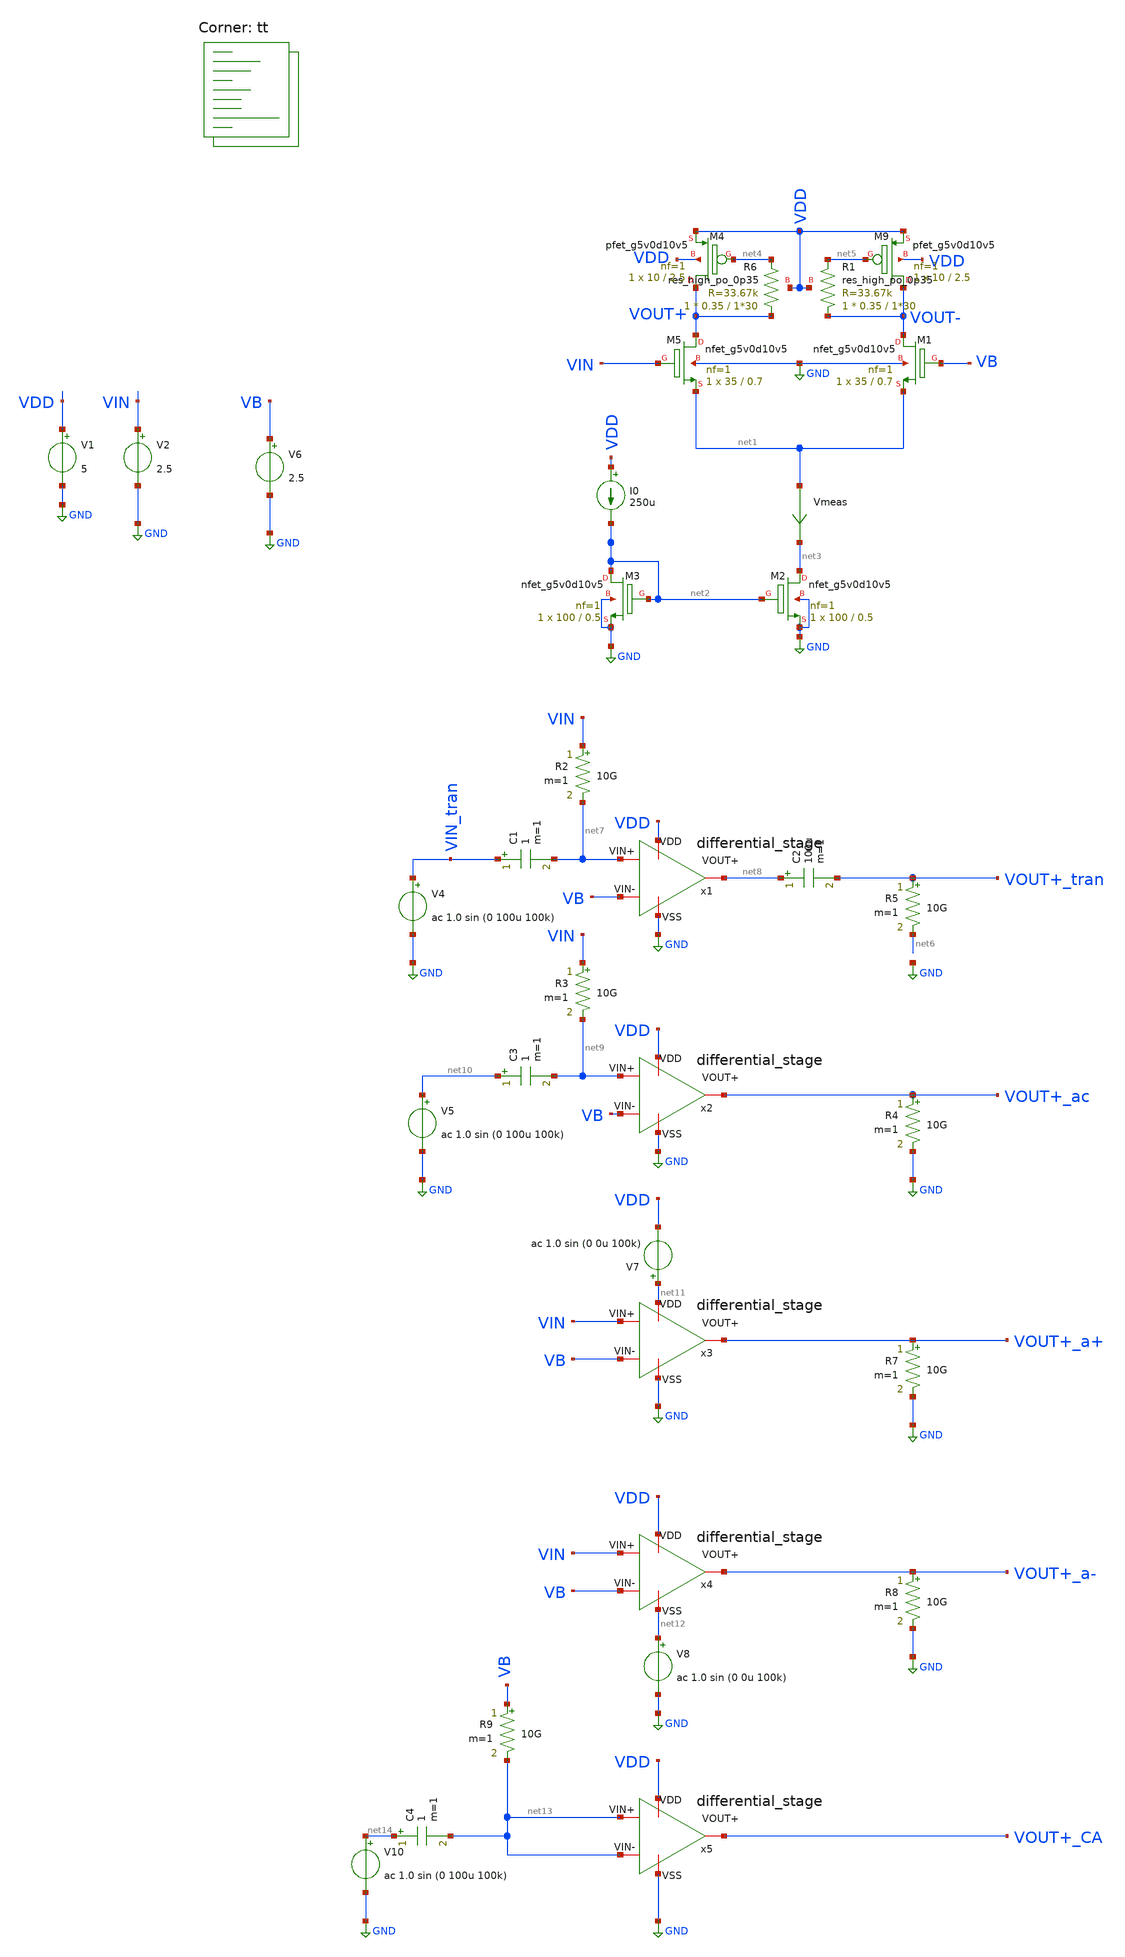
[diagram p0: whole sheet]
** sch_path: amplifiers/differencial_stage_amps/basic_stages/basic_NMOS_dif_stage/diferential_stage.sch
**.subckt diferential_stage
XM5 VOUT+ VIN net1 GND sky130_fd_pr__nfet_g5v0d10v5 L=0.7 W=35 nf=1 ad='int((1 + 1)/2) * 35 / 1 * 0.29'
+ as='int((1 + 2)/2) * 35 / 1 * 0.29' pd='2*int((1 + 1)/2) * (35 / 1 + 0.29)' ps='2*int((1 + 2)/2) * (35 / 1 + 0.29)'
+ nrd='0.29 / 35 ' nrs='0.29 / 35 ' sa=0 sb=0 sd=0 mult=1 m=1
XM1 VOUT- VB net1 GND sky130_fd_pr__nfet_g5v0d10v5 L=0.7 W=35 nf=1 ad='int((1 + 1)/2) * 35 / 1 * 0.29'
+ as='int((1 + 2)/2) * 35 / 1 * 0.29' pd='2*int((1 + 1)/2) * (35 / 1 + 0.29)' ps='2*int((1 + 2)/2) * (35 / 1 + 0.29)'
+ nrd='0.29 / 35 ' nrs='0.29 / 35 ' sa=0 sb=0 sd=0 mult=1 m=1
V1 VDD GND 5
V2 VIN GND 2.5
V6 VB GND 2.5
XM2 net3 net2 GND GND sky130_fd_pr__nfet_g5v0d10v5 L=0.5 W=100 nf=1 ad='int((1 + 1)/2) * 100 / 1 * 0.29'
+ as='int((1 + 2)/2) * 100 / 1 * 0.29' pd='2*int((1 + 1)/2) * (100 / 1 + 0.29)' ps='2*int((1 + 2)/2) * (100 / 1 + 0.29)'
+ nrd='0.29 / 100 ' nrs='0.29 / 100 ' sa=0 sb=0 sd=0 mult=1 m=1
Vmeas net1 net3 0
.save i(vmeas)
XM3 net2 net2 GND GND sky130_fd_pr__nfet_g5v0d10v5 L=0.5 W=100 nf=1 ad='int((1 + 1)/2) * 100 / 1 * 0.29'
+ as='int((1 + 2)/2) * 100 / 1 * 0.29' pd='2*int((1 + 1)/2) * (100 / 1 + 0.29)' ps='2*int((1 + 2)/2) * (100 / 1 + 0.29)'
+ nrd='0.29 / 100 ' nrs='0.29 / 100 ' sa=0 sb=0 sd=0 mult=1 m=1
I0 VDD net2 250u
XR6 VOUT+ net4 VDD sky130_fd_pr__res_high_po_0p35 L=1*30 mult=1 m=1
XR1 VOUT- net5 VDD sky130_fd_pr__res_high_po_0p35 L=1*30 mult=1 m=1
XM9 VOUT- net5 VDD VDD sky130_fd_pr__pfet_g5v0d10v5 L=2.5 W=10 nf=1 ad='int((1 + 1)/2) * 10 / 1 * 0.29'
+ as='int((1 + 2)/2) * 10 / 1 * 0.29' pd='2*int((1 + 1)/2) * (10 / 1 + 0.29)' ps='2*int((1 + 2)/2) * (10 / 1 + 0.29)'
+ nrd='0.29 / 10 ' nrs='0.29 / 10 ' sa=0 sb=0 sd=0 mult=1 m=1
XM4 VOUT+ net4 VDD VDD sky130_fd_pr__pfet_g5v0d10v5 L=2.5 W=10 nf=1 ad='int((1 + 1)/2) * 10 / 1 * 0.29'
+ as='int((1 + 2)/2) * 10 / 1 * 0.29' pd='2*int((1 + 1)/2) * (10 / 1 + 0.29)' ps='2*int((1 + 2)/2) * (10 / 1 + 0.29)'
+ nrd='0.29 / 10 ' nrs='0.29 / 10 ' sa=0 sb=0 sd=0 mult=1 m=1
R5 VOUT+_tran net6 10G m=1
R2 VIN net7 10G m=1
V4 VIN_tran GND ac 1.0 sin (0 100u 100k)
C2 net8 VOUT+_tran 100u m=1
C1 VIN_tran net7 1 m=1
R3 VIN net9 10G m=1
C3 net10 net9 1 m=1
V5 net10 GND ac 1.0 sin (0 100u 100k)
R4 VOUT+_ac GND 10G m=1
V7 net11 VDD ac 1.0 sin (0 0u 100k)
R7 VOUT+_a+ GND 10G m=1
V8 net12 GND ac 1.0 sin (0 0u 100k)
R8 VOUT+_a- GND 10G m=1
R9 VB net13 10G m=1
C4 net14 net13 1 m=1
V10 net14 GND ac 1.0 sin (0 100u 100k)
x1 VDD GND net7 VB net8 differential_stage
x2 VDD GND net9 VB VOUT+_ac differential_stage
x3 net11 GND VIN VB VOUT+_a+ differential_stage
x4 VDD net12 VIN VB VOUT+_a- differential_stage
x5 VDD GND net13 net13 VOUT+_CA differential_stage
**** begin user architecture code

**************************************************************
**************************************************************
**************************************************************
**************************************************************
**************************************************************
*LIBs*********************************************************
**************************************************************
**************************************************************
**************************************************************
**************************************************************
**************************************************************
*.lib $::SKYWATER_MODELS/sky130.lib.spice tt
* chose the corners in the corner file
* tt_mm for mismatch
* ss ff sf fs standart corners
* ll hh lh hl capacitor and resistors corners
* mc for total process variation including corners
**************************************************************
**************************************************************
**************************************************************
**************************************************************
**************************************************************
*Corners/montecarlo options***********************************
**************************************************************
**************************************************************
**************************************************************
**************************************************************
**************************************************************
.TEMP 27
**************************************************************
**************************************************************
**************************************************************
**************************************************************
*SIMULATION and Plots*****************************************
**************************************************************
**************************************************************
**************************************************************
**************************************************************
.control
save all
dc V2 0 5 0.01
*dc simulation
plot v(VOUT-) v(VIN) deriv(v(VOUT-)) v(VOUT+) deriv(v(VOUT+))
*ploting VIN VOUT and the voltage gain
plot i(Vmeas)
*ploting the current for curiosity
tran 1ns 20u
*transient simulation
plot (v(VOUT+_tran)) v(VIN_tran)
*simple plot to exemplify the gain
fft v(VOUT+_tran) v(VIN_tran)
*fast fourier transfor
plot mag(v(VOUT+_tran)) mag(v(VIN_tran))
ac dec 20 1 1000G
*simple ac simulation
plot db(v(VOUT+_ac))
plot db(v(VOUT+_a+))
plot db(v(VOUT+_a-))
plot db(v(VOUT+_CA))
plot db((v(VOUT+_ac))/(v(VOUT+_CA)))
plot db((v(VOUT+_ac))/(v(VOUT+_a+)))
plot db((v(VOUT+_ac))/(v(VOUT+_a-)))
.endc

.lib $::SKYWATER_MODELS/sky130.lib.spice tt
**** end user architecture code
**.ends
.GLOBAL GND
.end
